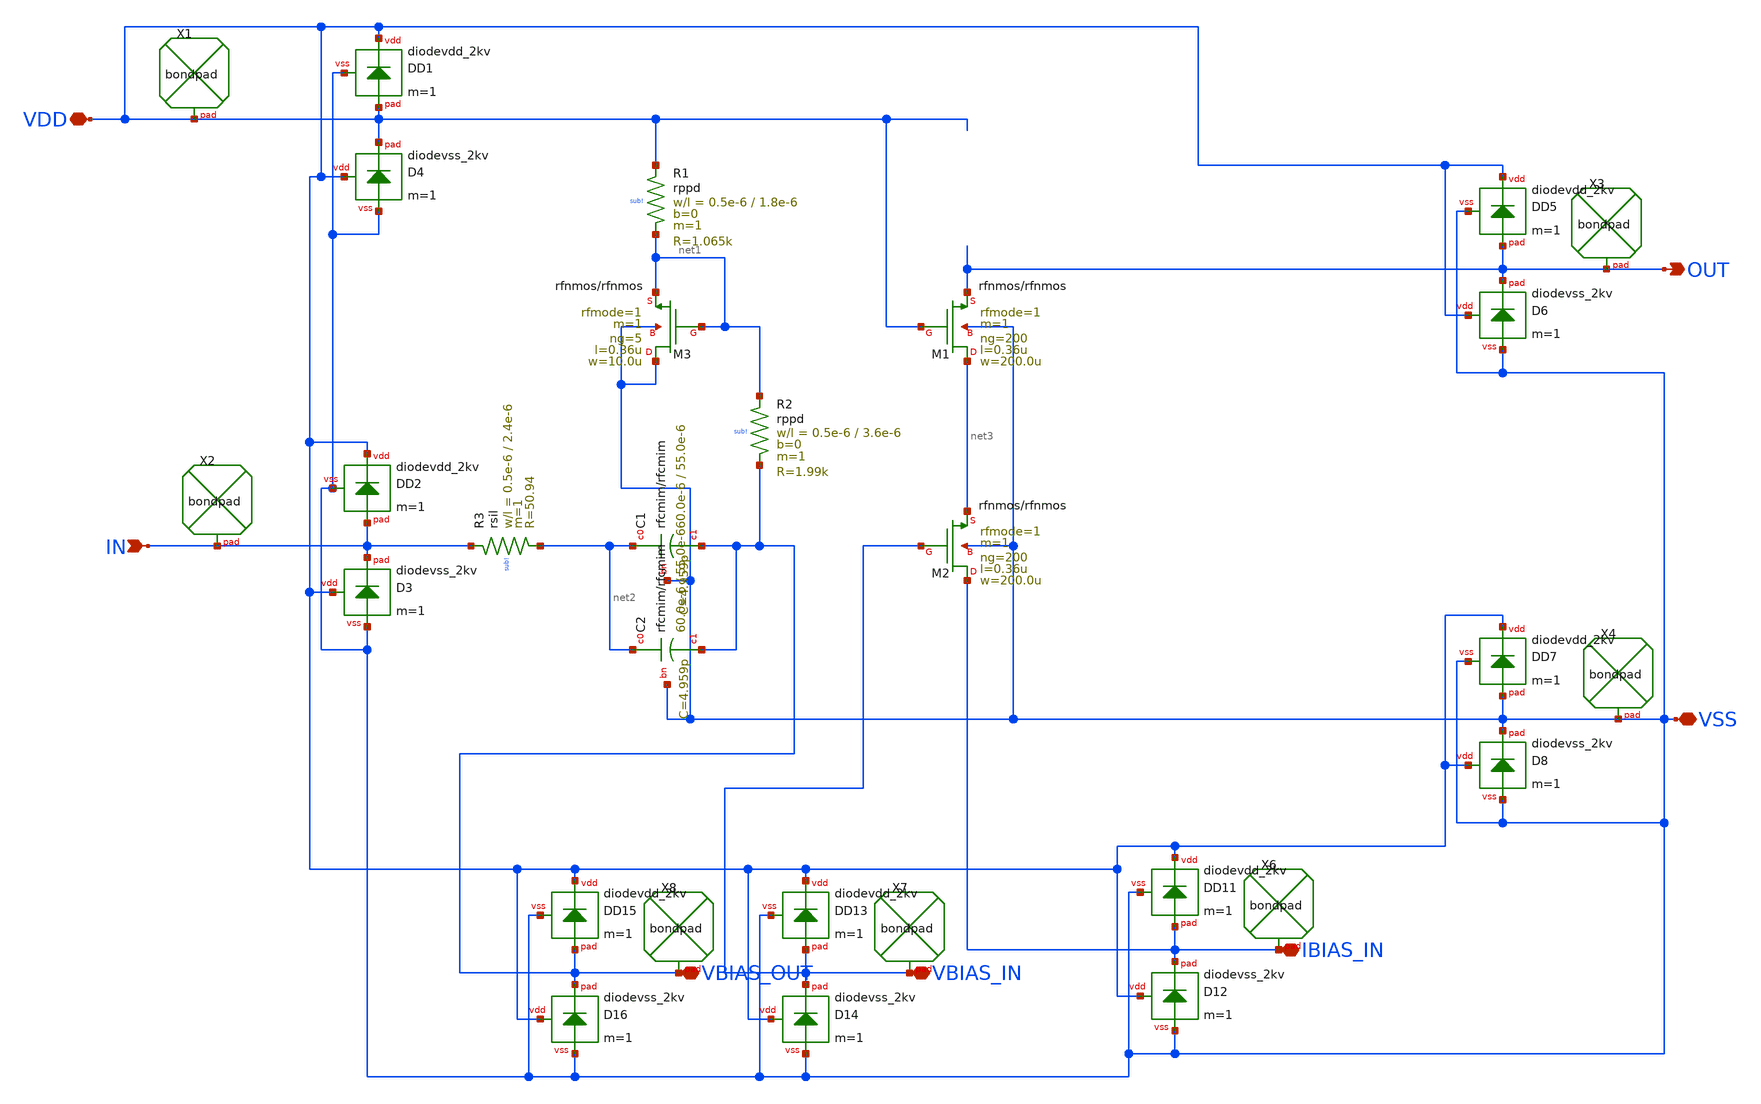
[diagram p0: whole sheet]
** sch_path: GPS_LNA/design_data/xschem/lna_nmos_pad.sch
**.subckt lna_nmos_pad VDD IN OUT VSS VBIAS_IN VBIAS_OUT IBIAS_IN
*.iopin VDD
*.ipin IN
*.opin OUT
*.iopin VSS
*.iopin VBIAS_IN
*.iopin VBIAS_OUT
*.iopin IBIAS_IN
XR2 net1 VBIAS_OUT sub! rppd w=0.5e-6 l=3.6e-6 m=1 b=0 mm_ok=1
XR1 VDD net1 sub! rppd w=0.5e-6 l=1.8e-6 m=1 b=0 mm_ok=1
XR3 IN net2 sub! rsil w=0.5e-6 l=2.4e-6 m=1 mm_ok=1
XC1 net2 VBIAS_OUT VSS rfcmim w=60.0e-6 l=55.0e-6 wfeed=5.0e-6 m=1 mm_ok=1
XC2 net2 VBIAS_OUT VSS rfcmim w=60.0e-6 l=55.0e-6 wfeed=5.0e-6 m=1 mm_ok=1
XM3 VSS net1 net1 VSS rfnmos w=10.0u l=0.36u ng=5 m=1 rfmode=1 mm_ok=1
XX1 VDD bondpad size=100u shape=0 padtype=0
XX3 OUT bondpad size=100u shape=0 padtype=0
XX4 VSS bondpad size=100u shape=0 padtype=0
XD1 VDD VDD VSS diodevdd_2kv m=1
XD4 VDD VDD VSS diodevss_2kv m=1
XX2 IN bondpad size=100u shape=0 padtype=0
XD2 VDD IN VSS diodevdd_2kv m=1
XD3 VDD IN VSS diodevss_2kv m=1
XD5 VDD OUT VSS diodevdd_2kv m=1
XD6 VDD OUT VSS diodevss_2kv m=1
XD7 VDD VSS VSS diodevdd_2kv m=1
XD8 VDD VSS VSS diodevss_2kv m=1
XX6 IBIAS_IN bondpad size=100u shape=0 padtype=0
XD11 VDD IBIAS_IN VSS diodevdd_2kv m=1
XD12 VDD IBIAS_IN VSS diodevss_2kv m=1
XX7 VBIAS_IN bondpad size=100u shape=0 padtype=0
XD13 VDD VBIAS_IN VSS diodevdd_2kv m=1
XD14 VDD VBIAS_IN VSS diodevss_2kv m=1
XX8 VBIAS_OUT bondpad size=100u shape=0 padtype=0
XD15 VDD VBIAS_OUT VSS diodevdd_2kv m=1
XD16 VDD VBIAS_OUT VSS diodevss_2kv m=1
XM1 net3 VDD OUT VSS rfnmos w=200.0u l=0.36u ng=200 m=1 rfmode=1 mm_ok=1
XM2 IBIAS_IN VBIAS_IN net3 VSS rfnmos w=200.0u l=0.36u ng=200 m=1 rfmode=1 mm_ok=1
**.ends
.end
